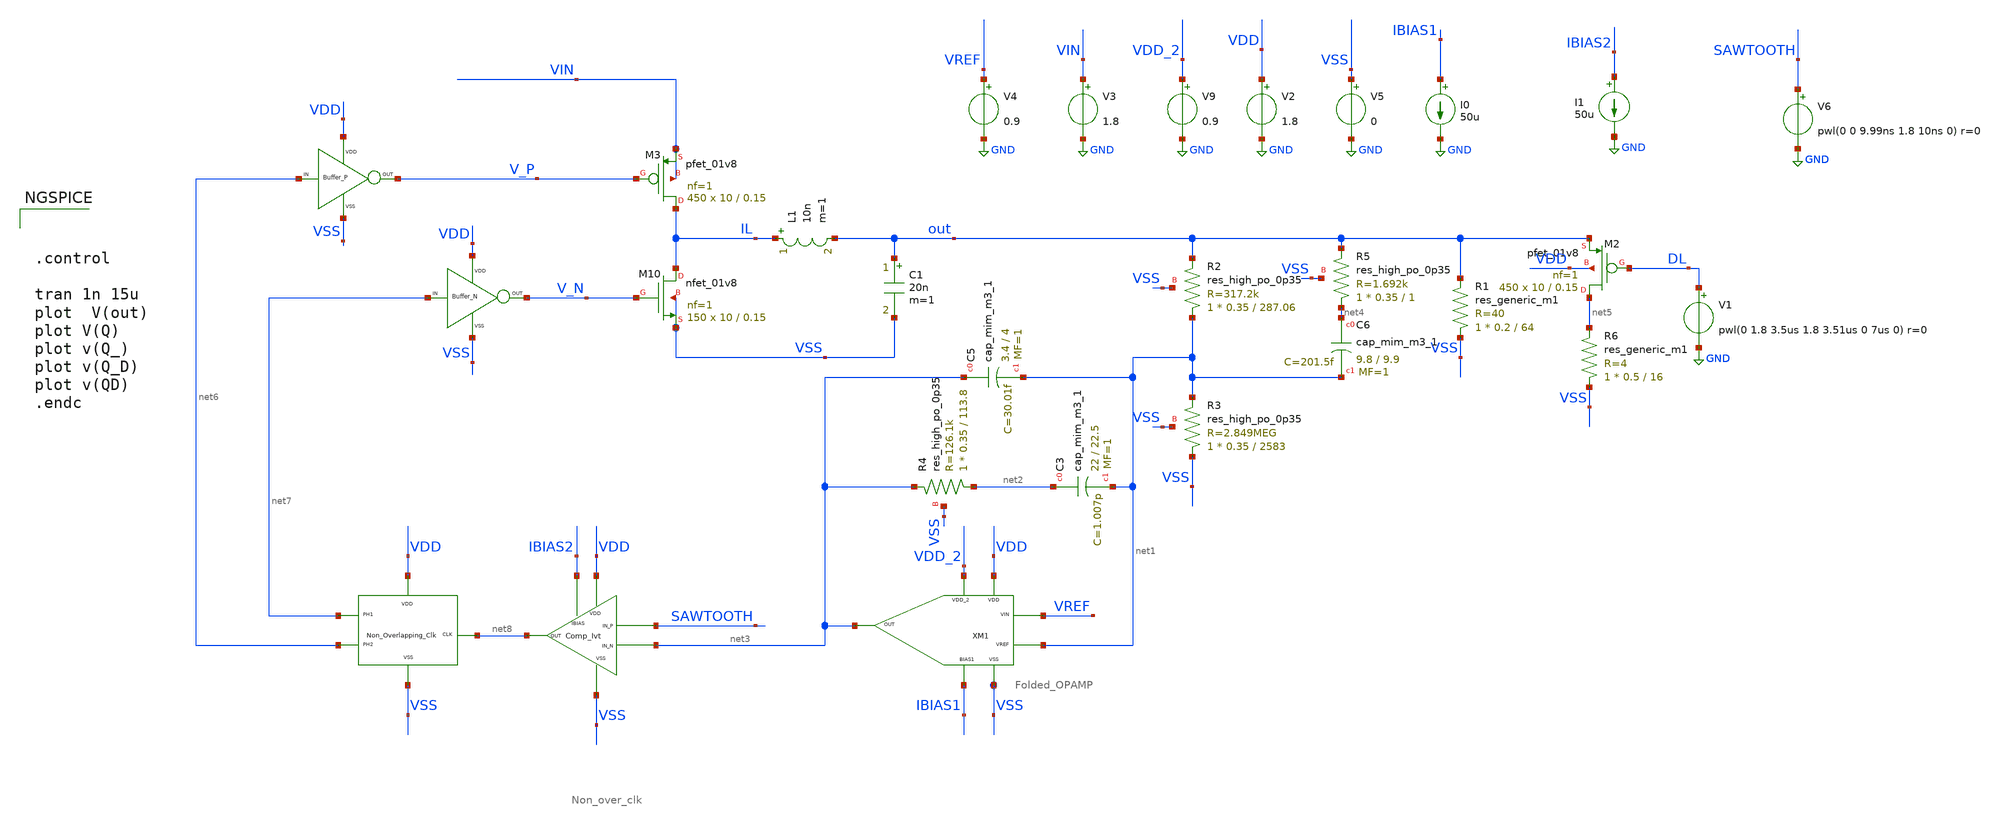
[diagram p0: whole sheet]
** sch_path: xschem/DC_DC_Converter_xschem/OTHERS/DC_DC_Converter_JV8/TOP_LEVEL/closed_loop_v12.sch
**.subckt closed_loop_v12
XM3 IL V_P VIN VIN sky130_fd_pr__pfet_01v8 L=0.15 W=10 nf=1 ad='int((nf+1)/2) * W/nf * 0.29' as='int((nf+2)/2) * W/nf * 0.29'
+ pd='2*int((nf+1)/2) * (W/nf + 0.29)' ps='2*int((nf+2)/2) * (W/nf + 0.29)' nrd='0.29 / W' nrs='0.29 / W'
+ sa=0 sb=0 sd=0 mult=450 m=450
L1 IL out 10n m=1
C1 out VSS 20n m=1
V3 VIN GND 1.8
I0 IBIAS1 GND 50u
V9 VDD_2 GND 0.9
V2 VDD GND 1.8
V5 VSS GND 0
V4 VREF GND 0.9
I1 IBIAS2 GND 50u
V6 SAWTOOTH GND pwl(0 0 9.99ns 1.8 10ns 0) r=0
XM2 net5 DL out VDD sky130_fd_pr__pfet_01v8 L=0.15 W=10 nf=1 ad='int((nf+1)/2) * W/nf * 0.29' as='int((nf+2)/2) * W/nf * 0.29'
+ pd='2*int((nf+1)/2) * (W/nf + 0.29)' ps='2*int((nf+2)/2) * (W/nf + 0.29)' nrd='0.29 / W' nrs='0.29 / W'
+ sa=0 sb=0 sd=0 mult=450 m=450
V1 DL GND pwl(0 1.8 3.5us 1.8 3.51us 0 7us 0) r=0
X1 net6 V_P VDD VSS BUFFER_P
X2 net7 V_N VDD VSS BUFFER_N
xM3 VDD net8 net7 VSS net6 Non_over_clk
XC5 net3 net1 sky130_fd_pr__cap_mim_m3_1 W=3.4 L=4 MF=1 m=1
XC3 net2 net1 sky130_fd_pr__cap_mim_m3_1 W=22 L=22.5 MF=1 m=1
R6 VSS net5 sky130_fd_pr__res_generic_m1 W=0.5 L=16 m=1
R1 VSS out sky130_fd_pr__res_generic_m1 W=0.2 L=64 m=1
XC6 net4 net1 sky130_fd_pr__cap_mim_m3_1 W=9.8 L=9.9 MF=1 m=1
XM10 IL V_N VSS VSS sky130_fd_pr__nfet_01v8 L=0.15 W=10 nf=1 ad='int((nf+1)/2) * W/nf * 0.29' as='int((nf+2)/2) * W/nf * 0.29'
+ pd='2*int((nf+1)/2) * (W/nf + 0.29)' ps='2*int((nf+2)/2) * (W/nf + 0.29)' nrd='0.29 / W' nrs='0.29 / W'
+ sa=0 sb=0 sd=0 mult=150 m=150
XM2 IBIAS2 VDD SAWTOOTH net3 VSS net8 Comp_lvt
XR4 net2 net3 VSS sky130_fd_pr__res_high_po_0p35 L=113.8 mult=1 m=1
XR5 net4 out VSS sky130_fd_pr__res_high_po_0p35 L=1 mult=1 m=1
XR2 net1 out VSS sky130_fd_pr__res_high_po_0p35 L=287.06 mult=1 m=1
XR3 VSS net1 VSS sky130_fd_pr__res_high_po_0p35 L=2583 mult=1 m=1
XM1 VDD VSS VDD_2 IBIAS1 net3 VREF net1 Folded_OPAMP
**** begin user architecture code

** opencircuitdesign pdks install
.lib $::SKYWATER_MODELS/sky130.lib.spice tt





.control

tran 1n 15u
plot  V(out)
plot V(Q)
plot v(Q_)
plot v(Q_D)
plot v(QD)
.endc


**** end user architecture code
**.ends
.GLOBAL GND
.end
